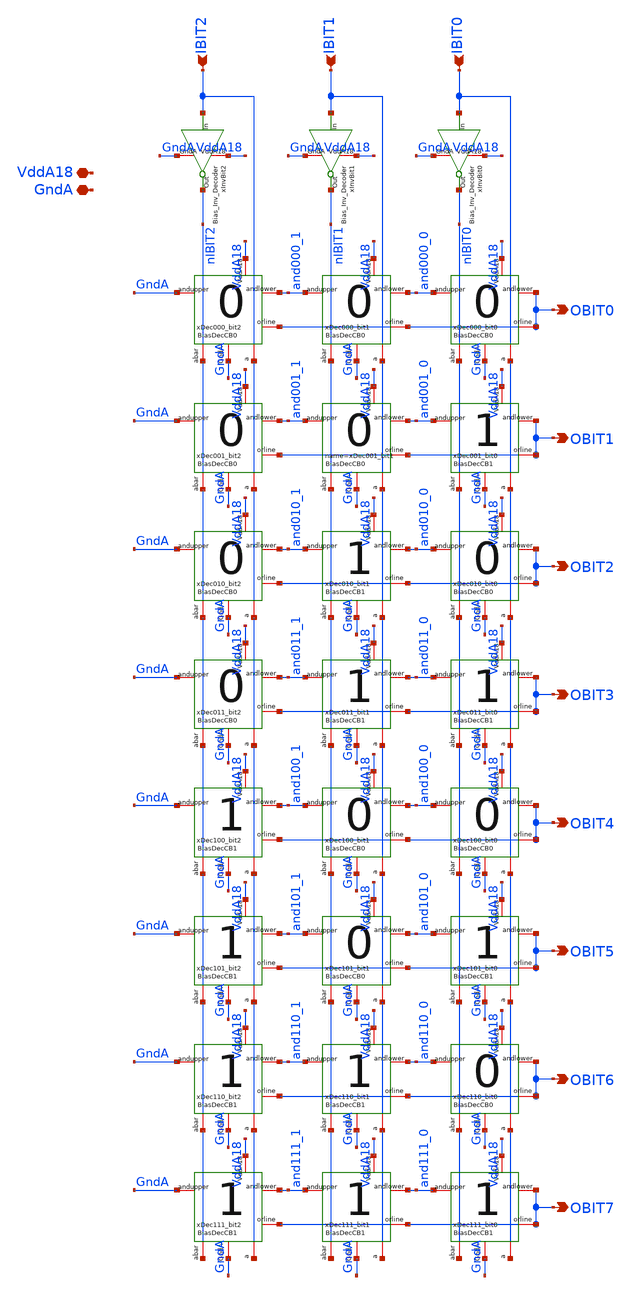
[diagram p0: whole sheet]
** sch_path: analog/xschem/BiasDec3to8.sch
**.subckt BiasDec3to8 GndA VddA18 IBIT2 IBIT1 IBIT0 OBIT0 OBIT1 OBIT2 OBIT3 OBIT4 OBIT5 OBIT6 OBIT7
*.iopin GndA
*.iopin VddA18
*.ipin IBIT2
*.ipin IBIT1
*.ipin IBIT0
*.opin OBIT0
*.opin OBIT1
*.opin OBIT2
*.opin OBIT3
*.opin OBIT4
*.opin OBIT5
*.opin OBIT6
*.opin OBIT7
xDec000_bit2 OBIT0 and000_1 GndA GndA VddA18 IBIT2 nIBIT2 BiasDecCB0
xDec001_bit0 OBIT1 OBIT1 and001_0 GndA VddA18 IBIT0 nIBIT0 BiasDecCB1
xDec000_bit1 OBIT0 and000_0 and000_1 GndA VddA18 IBIT1 nIBIT1 BiasDecCB0
xDec000_bit0 OBIT0 OBIT0 and000_0 GndA VddA18 IBIT0 nIBIT0 BiasDecCB0
name=xDec001_bit1 OBIT1 and001_0 and001_1 GndA VddA18 IBIT1 nIBIT1 BiasDecCB0
xDec001_bit2 OBIT1 and001_1 GndA GndA VddA18 IBIT2 nIBIT2 BiasDecCB0
xDec010_bit2 OBIT2 and010_1 GndA GndA VddA18 IBIT2 nIBIT2 BiasDecCB0
xDec011_bit0 OBIT3 OBIT3 and011_0 GndA VddA18 IBIT0 nIBIT0 BiasDecCB1
xDec010_bit0 OBIT2 OBIT2 and010_0 GndA VddA18 IBIT0 nIBIT0 BiasDecCB0
xDec011_bit1 OBIT3 and011_0 and011_1 GndA VddA18 IBIT1 nIBIT1 BiasDecCB1
xDec011_bit2 OBIT3 and011_1 GndA GndA VddA18 IBIT2 nIBIT2 BiasDecCB0
xDec100_bit2 OBIT4 and100_1 GndA GndA VddA18 IBIT2 nIBIT2 BiasDecCB1
xDec101_bit0 OBIT5 OBIT5 and101_0 GndA VddA18 IBIT0 nIBIT0 BiasDecCB1
xDec100_bit1 OBIT4 and100_0 and100_1 GndA VddA18 IBIT1 nIBIT1 BiasDecCB0
xDec100_bit0 OBIT4 OBIT4 and100_0 GndA VddA18 IBIT0 nIBIT0 BiasDecCB0
xDec101_bit1 OBIT5 and101_0 and101_1 GndA VddA18 IBIT1 nIBIT1 BiasDecCB0
xDec101_bit2 OBIT5 and101_1 GndA GndA VddA18 IBIT2 nIBIT2 BiasDecCB1
xDec110_bit2 OBIT6 and110_1 GndA GndA VddA18 IBIT2 nIBIT2 BiasDecCB1
xDec111_bit0 OBIT7 OBIT7 and111_0 GndA VddA18 IBIT0 nIBIT0 BiasDecCB1
xDec110_bit1 OBIT6 and110_0 and110_1 GndA VddA18 IBIT1 nIBIT1 BiasDecCB1
xDec110_bit0 OBIT6 OBIT6 and110_0 GndA VddA18 IBIT0 nIBIT0 BiasDecCB0
xDec111_bit1 OBIT7 and111_0 and111_1 GndA VddA18 IBIT1 nIBIT1 BiasDecCB1
xDec111_bit2 OBIT7 and111_1 GndA GndA VddA18 IBIT2 nIBIT2 BiasDecCB1
xDec010_bit1 OBIT2 and010_0 and010_1 GndA VddA18 IBIT1 nIBIT1 BiasDecCB1
xInvBit2 VddA18 GndA nIBIT2 IBIT2 Bias_Inv_Decoder
xInvBit1 VddA18 GndA nIBIT1 IBIT1 Bias_Inv_Decoder
xInvBit0 VddA18 GndA nIBIT0 IBIT0 Bias_Inv_Decoder
**.ends
.end
